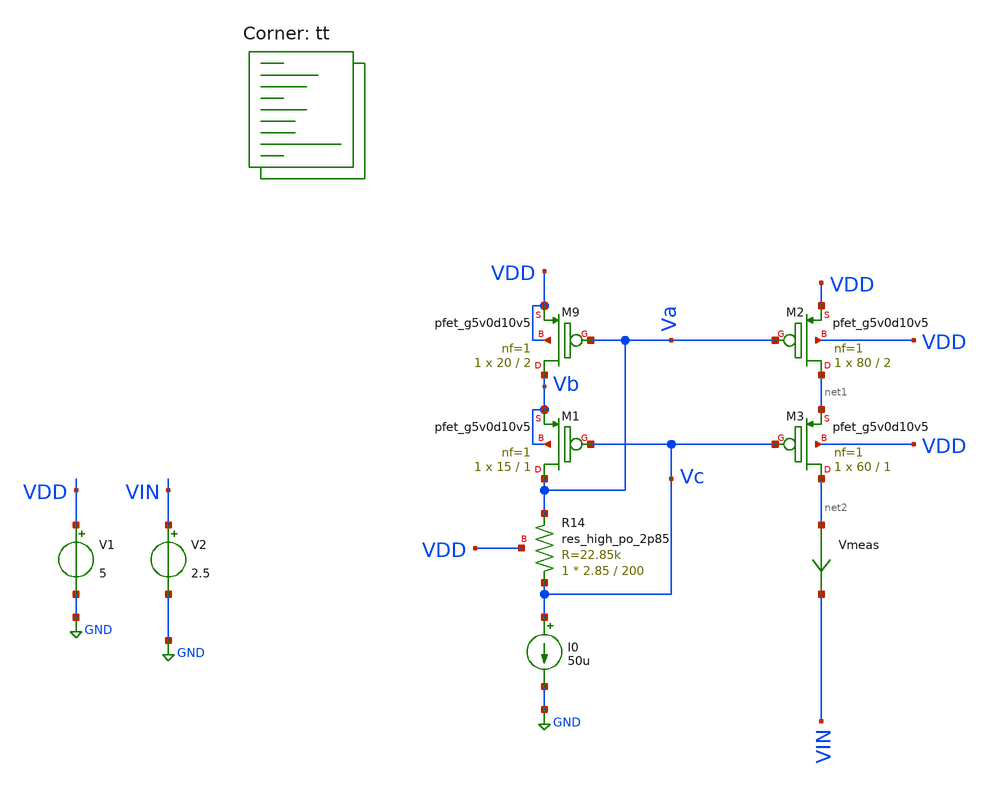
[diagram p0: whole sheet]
** sch_path: old stuff/my_amp_test/second stage/current_mirror_test.sch
**.subckt current_mirror_test
V1 VDD GND 5
V2 VIN GND 2.5
I0 Vc GND 50u
XM9 Vb Va VDD VDD sky130_fd_pr__pfet_g5v0d10v5 L=2 W=20 nf=1 ad='int((1 + 1)/2) * 20 / 1 * 0.29' as='int((1 + 2)/2) * 20 / 1 * 0.29'
+ pd='2*int((1 + 1)/2) * (20 / 1 + 0.29)' ps='2*int((1 + 2)/2) * (20 / 1 + 0.29)' nrd='0.29 / 20 ' nrs='0.29 / 20 '
+ sa=0 sb=0 sd=0 mult=1 m=1
XM1 Va Vc Vb Vb sky130_fd_pr__pfet_g5v0d10v5 L=1 W=15 nf=1 ad='int((1 + 1)/2) * 15 / 1 * 0.29' as='int((1 + 2)/2) * 15 / 1 * 0.29'
+ pd='2*int((1 + 1)/2) * (15 / 1 + 0.29)' ps='2*int((1 + 2)/2) * (15 / 1 + 0.29)' nrd='0.29 / 15 ' nrs='0.29 / 15 '
+ sa=0 sb=0 sd=0 mult=1 m=1
XR14 Vc Va VDD sky130_fd_pr__res_high_po_2p85 L=200 mult=1 m=1
Vmeas net2 VIN 0
.save i(vmeas)
XM2 net1 Va VDD VDD sky130_fd_pr__pfet_g5v0d10v5 L=2 W=80 nf=1 ad='int((1 + 1)/2) * 80 / 1 * 0.29' as='int((1 + 2)/2) * 80 / 1 * 0.29'
+ pd='2*int((1 + 1)/2) * (80 / 1 + 0.29)' ps='2*int((1 + 2)/2) * (80 / 1 + 0.29)' nrd='0.29 / 80 ' nrs='0.29 / 80 '
+ sa=0 sb=0 sd=0 mult=1 m=1
XM3 net2 Vc net1 VDD sky130_fd_pr__pfet_g5v0d10v5 L=1 W=60 nf=1 ad='int((1 + 1)/2) * 60 / 1 * 0.29' as='int((1 + 2)/2) * 60 / 1 * 0.29'
+ pd='2*int((1 + 1)/2) * (60 / 1 + 0.29)' ps='2*int((1 + 2)/2) * (60 / 1 + 0.29)' nrd='0.29 / 60 ' nrs='0.29 / 60 '
+ sa=0 sb=0 sd=0 mult=1 m=1
**** begin user architecture code
.lib $::SKYWATER_MODELS/sky130.lib.spice tt

**************************************************************
**************************************************************
**************************************************************
**************************************************************
**************************************************************
*LIBs*********************************************************
**************************************************************
**************************************************************
**************************************************************
**************************************************************
**************************************************************
*.lib $::SKYWATER_MODELS/sky130.lib.spice tt
* chose the corners in the corner file
* tt_mm for mismatch
* ss ff sf fs standart corners
* ll hh lh hl capacitor and resistors corners
* mc for total process variation including corners
**************************************************************
**************************************************************
**************************************************************
**************************************************************
**************************************************************
*Corners/montecarlo options***********************************
**************************************************************
**************************************************************
**************************************************************
**************************************************************
**************************************************************
.TEMP 27
**************************************************************
**************************************************************
**************************************************************
**************************************************************
*SIMULATION and Plots*****************************************
**************************************************************
**************************************************************
**************************************************************
**************************************************************
.control
save all
dc V2 0 5 0.001
*dc simulation
*ploting VIN VOUT and the voltage gain
plot i(Vmeas)
plot 1/deriv(i(Vmeas))
plot v(Va) v(Vb) v(Vc)
.endc

**** end user architecture code
**.ends
.GLOBAL GND
.end
